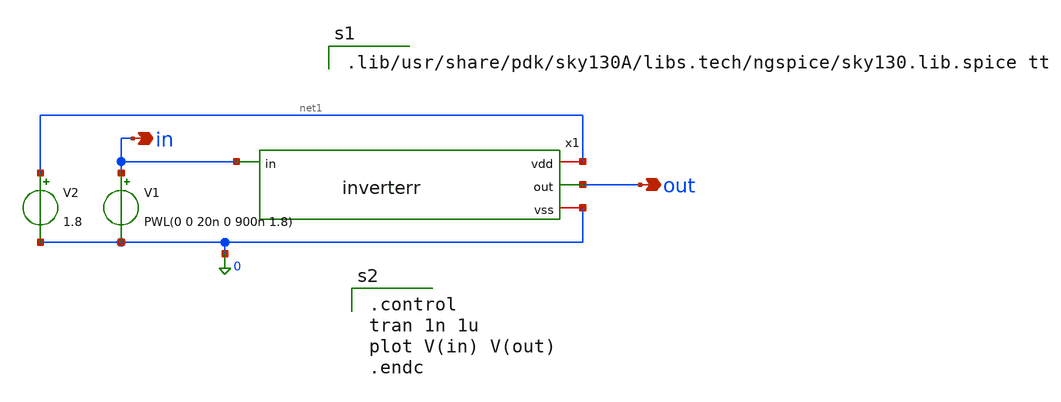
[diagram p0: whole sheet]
** sch_path: Lab1_and/xschem/inverterr_tb.sch
**.subckt inverterr_tb in out
*.opin in
*.opin out
x1 net1 out in 0 inverterr
V1 in 0 PWL(0 0 20n 0 900n 1.8)
V2 net1 0 1.8
**** begin user architecture code

.lib/usr/share/pdk/sky130A/libs.tech/ngspice/sky130.lib.spice tt


.control
tran 1n 1u
plot V(in) V(out)
.endc

**** end user architecture code
**.ends

* expanding   symbol:  inverterr.sym # of pins=4
** sym_path: Lab1_and/xschem/inverterr.sym
** sch_path: Lab1_and/xschem/inverterr.sch
.subckt inverterr vdd out in vss
*.ipin in
*.iopin vss
*.opin out
*.iopin vdd
XM1 out in vss vss sky130_fd_pr__nfet_01v8 L=0.18 W=4.5 nf=3 ad='int((3 + 1)/2) * 4.5 / 3 * 0.29' as='int((3 + 2)/2) * 4.5 / 3 * 0.29'
+ pd='2*int((3 + 1)/2) * (4.5 / 3 + 0.29)' ps='2*int((3 + 2)/2) * (4.5 / 3 + 0.29)' nrd='0.29 / 4.5 ' nrs='0.29 / 4.5 '
+ sa=0 sb=0 sd=0 mult=1 m=1
XM2 out in vdd vdd sky130_fd_pr__pfet_01v8 L=0.18 W=3 nf=3 ad='int((3 + 1)/2) * 3 / 3 * 0.29' as='int((3 + 2)/2) * 3 / 3 * 0.29'
+ pd='2*int((3 + 1)/2) * (3 / 3 + 0.29)' ps='2*int((3 + 2)/2) * (3 / 3 + 0.29)' nrd='0.29 / 3 ' nrs='0.29 / 3 '
+ sa=0 sb=0 sd=0 mult=1 m=1
.ends

.end
